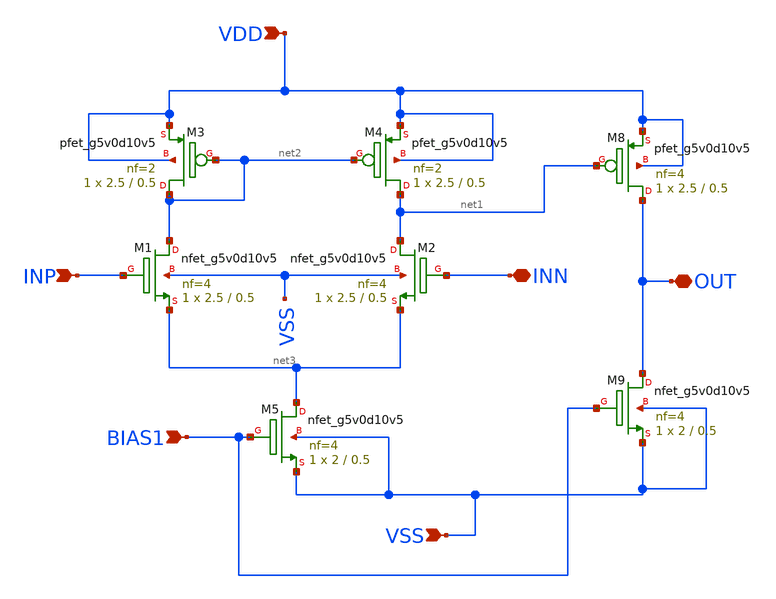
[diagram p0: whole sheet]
** sch_path: xschem/opamp.sch
**.subckt opamp INP BIAS1 VSS VDD INN OUT
*.ipin INP
*.ipin BIAS1
*.ipin VSS
*.ipin VDD
*.iopin INN
*.iopin OUT
XM3 net2 net2 VDD VDD sky130_fd_pr__pfet_g5v0d10v5 L=0.5 W=2.5 nf=2 ad='int((nf+1)/2) * W/nf * 0.29'
+ as='int((nf+2)/2) * W/nf * 0.29' pd='2*int((nf+1)/2) * (W/nf + 0.29)' ps='2*int((nf+2)/2) * (W/nf + 0.29)'
+ nrd='0.29 / W' nrs='0.29 / W' sa=0 sb=0 sd=0 mult=1 m=1
XM4 net1 net2 VDD VDD sky130_fd_pr__pfet_g5v0d10v5 L=0.5 W=2.5 nf=2 ad='int((nf+1)/2) * W/nf * 0.29'
+ as='int((nf+2)/2) * W/nf * 0.29' pd='2*int((nf+1)/2) * (W/nf + 0.29)' ps='2*int((nf+2)/2) * (W/nf + 0.29)'
+ nrd='0.29 / W' nrs='0.29 / W' sa=0 sb=0 sd=0 mult=1 m=1
XM1 net2 INP net3 VSS sky130_fd_pr__nfet_g5v0d10v5 L=0.5 W=2.5 nf=4 ad='int((nf+1)/2) * W/nf * 0.29'
+ as='int((nf+2)/2) * W/nf * 0.29' pd='2*int((nf+1)/2) * (W/nf + 0.29)' ps='2*int((nf+2)/2) * (W/nf + 0.29)'
+ nrd='0.29 / W' nrs='0.29 / W' sa=0 sb=0 sd=0 mult=1 m=1
XM2 net1 INN net3 VSS sky130_fd_pr__nfet_g5v0d10v5 L=0.5 W=2.5 nf=4 ad='int((nf+1)/2) * W/nf * 0.29'
+ as='int((nf+2)/2) * W/nf * 0.29' pd='2*int((nf+1)/2) * (W/nf + 0.29)' ps='2*int((nf+2)/2) * (W/nf + 0.29)'
+ nrd='0.29 / W' nrs='0.29 / W' sa=0 sb=0 sd=0 mult=1 m=1
XM5 net3 BIAS1 VSS VSS sky130_fd_pr__nfet_g5v0d10v5 L=0.5 W=2 nf=4 ad='int((nf+1)/2) * W/nf * 0.29' as='int((nf+2)/2) * W/nf * 0.29'
+ pd='2*int((nf+1)/2) * (W/nf + 0.29)' ps='2*int((nf+2)/2) * (W/nf + 0.29)' nrd='0.29 / W' nrs='0.29 / W'
+ sa=0 sb=0 sd=0 mult=1 m=1
XM8 OUT net1 VDD VDD sky130_fd_pr__pfet_g5v0d10v5 L=0.5 W=2.5 nf=4 ad='int((nf+1)/2) * W/nf * 0.29' as='int((nf+2)/2) * W/nf * 0.29'
+ pd='2*int((nf+1)/2) * (W/nf + 0.29)' ps='2*int((nf+2)/2) * (W/nf + 0.29)' nrd='0.29 / W' nrs='0.29 / W'
+ sa=0 sb=0 sd=0 mult=1 m=1
XM9 OUT BIAS1 VSS VSS sky130_fd_pr__nfet_g5v0d10v5 L=0.5 W=2 nf=4 ad='int((nf+1)/2) * W/nf * 0.29' as='int((nf+2)/2) * W/nf * 0.29'
+ pd='2*int((nf+1)/2) * (W/nf + 0.29)' ps='2*int((nf+2)/2) * (W/nf + 0.29)' nrd='0.29 / W' nrs='0.29 / W'
+ sa=0 sb=0 sd=0 mult=1 m=1
**.ends
.end
